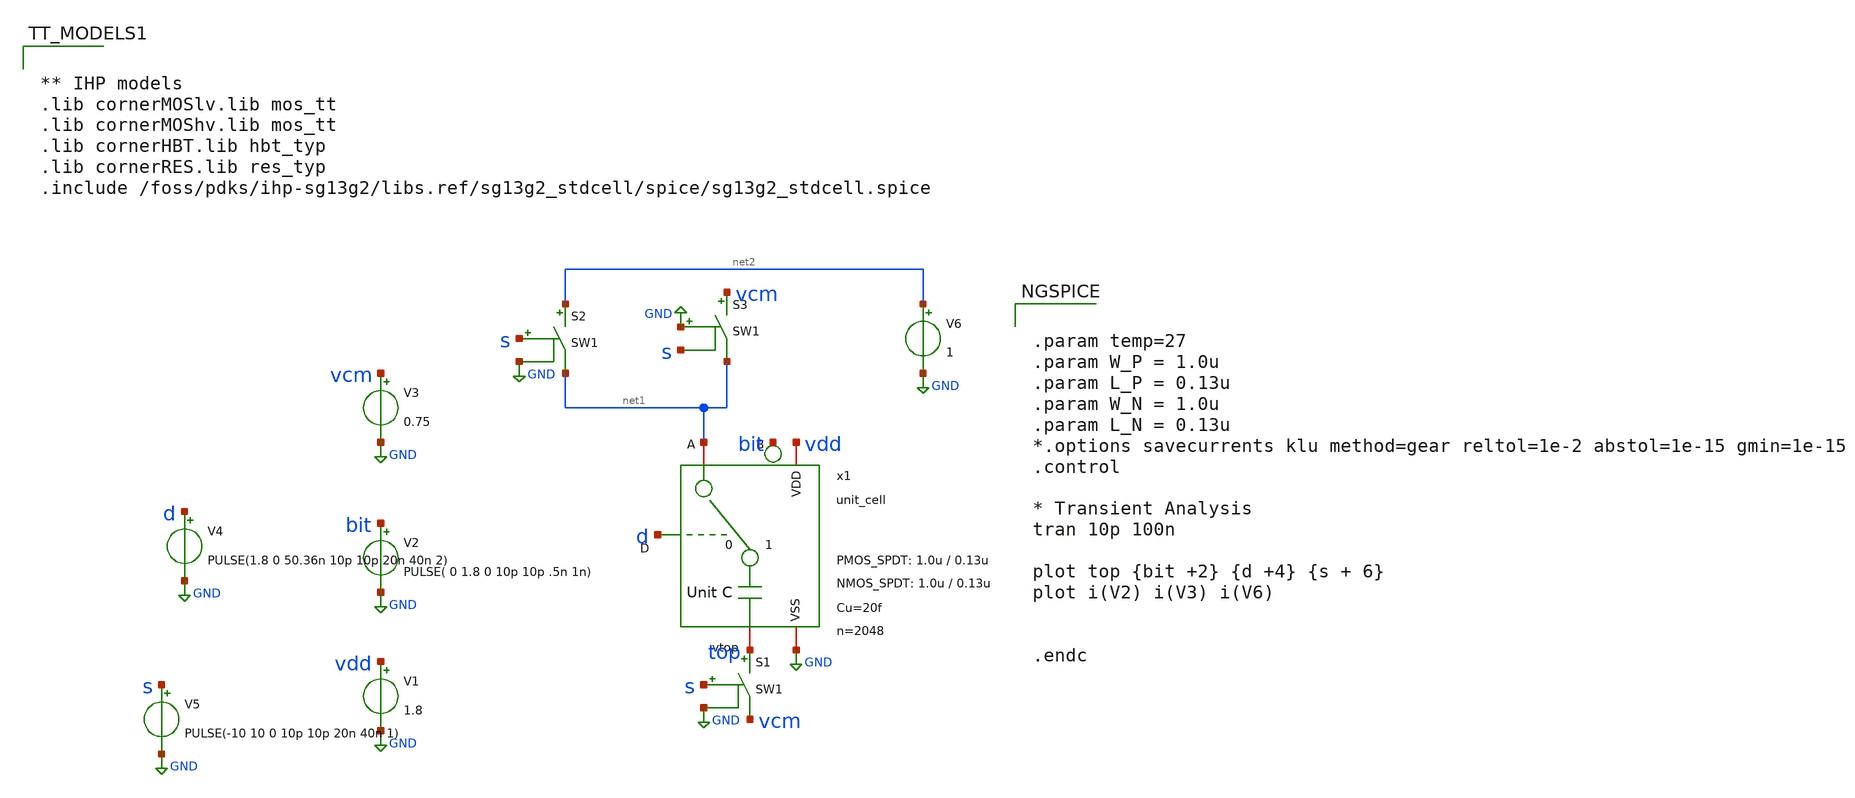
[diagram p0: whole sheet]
** sch_path: xschem/dac_icms_cell/testbenches/tb_unit_cell_tran.sch
* IHP-GmbH/IHP-Open-PDK/ihp-sg13g2/libs.tech/xschem/sg13g2_stdcells/sg13g2_dlygate4sd2_1.sch:
* Copyright 2023 IHP PDK Authors
* Licensed under the Apache License, Version 2.0 (the "License");
**.subckt tb_unit_cell_tran
x1 bit net1 GND d vdd top unit_cell W_P_SPDT=1.0u L_P_SPDT=0.13u W_N_SPDT=1.0u L_N_SPDT=0.13u Cu=20f
+ n=2048
V1 vdd GND 1.8
V2 bit GND PULSE( 0 1.8 0 10p 10p .5n 1n)
V3 vcm GND 0.75
V4 d GND PULSE(1.8 0 50.36n 10p 10p 20n 40n 2)
S1 top vcm s GND SW1
V5 s GND PULSE(-10 10 0 10p 10p 20n 40n 1)
S2 net2 net1 s GND SW1
S3 vcm net1 GND s SW1
V6 net2 GND 1
**** begin user architecture code


.param temp=27
.param W_P = 1.0u
.param L_P = 0.13u
.param W_N = 1.0u
.param L_N = 0.13u
*.options savecurrents klu method=gear reltol=1e-2 abstol=1e-15 gmin=1e-15
.control

* Transient Analysis
tran 10p 100n

plot top {bit +2} {d +4} {s + 6}
plot i(V2) i(V3) i(V6)


.endc




** IHP models
.lib cornerMOSlv.lib mos_tt
.lib cornerMOShv.lib mos_tt
.lib cornerHBT.lib hbt_typ
.lib cornerRES.lib res_typ
.include /foss/pdks/ihp-sg13g2/libs.ref/sg13g2_stdcell/spice/sg13g2_stdcell.spice


**** end user architecture code
**.ends

* expanding   symbol:  dac_icms_cell/unit_cell.sym # of pins=6
** sym_path: xschem/dac_icms_cell/unit_cell.sym
** sch_path: xschem/dac_icms_cell/unit_cell.sch
.subckt unit_cell B A VSS D VDD vtop  W_P_SPDT=1.0u L_P_SPDT=0.13u W_N_SPDT=1.0u L_N_SPDT=0.13u
+ Cu=8f n=1
*.iopin VSS
*.iopin A
*.iopin VDD
*.ipin D
*.iopin B
*.iopin vtop
x1 VDD net3 VSS net1 net2 A dac_switch W_P_TG=3.0u L_P_TG=0.13u W_N_TG=1.0u L_N_TG=0.13u n={1}
C1 net1 vtop Cu m=n
x35 VDD B net2 VSS buffer_lv W_P_INV=10.0u L_P_INV=0.13u W_N_INV=10.0u L_N_INV=0.13u
x2 VDD D net3 VSS buffer_lv W_P_INV=10.0u L_P_INV=0.13u W_N_INV=10.0u L_N_INV=0.13u
.ends


* expanding   symbol:  dac_icms_cell/dac_switch.sym # of pins=6
** sym_path: xschem/dac_icms_cell/dac_switch.sym
** sch_path: xschem/dac_icms_cell/dac_switch.sch
.subckt dac_switch VDD di_spdt_ctrl VSS v_c v_b v_a  W_P_TG=3.0u L_P_TG=0.13u W_N_TG=1.0u
+ L_N_TG=0.13u n=1
*.iopin v_a
*.iopin v_c
*.iopin VDD
*.iopin VSS
*.ipin di_spdt_ctrl
*.iopin v_b
x1 VDD di_spdt_ctrl VSS v_c v_a di_spdt_ctrl_n transmission_gate_lv_w_dummy W_P=W_P_TG L_P=L_P_TG
+ W_N=W_N_TG L_N=L_N_TG W_P_D=1.0u L_P_D=0.13u W_N_D=1.0u L_N_D=0.13u n=n
x8 VDD di_spdt_ctrl di_spdt_ctrl_n VSS inverter_lv W_P=W_P_TG L_P=L_P_TG W_N=W_N_TG L_N=L_N_TG n=1
XM1 net1 v_b VSS VSS sg13_lv_nmos w=0.5u l=0.2u ng=1 m=n mm_ok=1
XM3 net1 v_b VDD VDD sg13_lv_pmos w=1u l=0.2u ng=1 m=n mm_ok=1
x2 VDD net2 VSS net1 v_c net3 transmission_gate_lv_w_dummy W_P=W_P_TG L_P=L_P_TG W_N=W_N_TG
+ L_N=L_N_TG W_P_D=1.0u L_P_D=0.13u W_N_D=1.0u L_N_D=0.13u n=n
x40 net2 di_spdt_ctrl_n VDD VSS sg13g2_dlygate4sd2_1
x4 net3 di_spdt_ctrl VDD VSS sg13g2_dlygate4sd2_1
.ends


* expanding   symbol:  buffer/buffer_lv.sym # of pins=4
** sym_path: buffer/buffer_lv.sym
** sch_path: buffer/buffer_lv.sch
.subckt buffer_lv VDD vin vout VSS  W_P_INV=3.0u L_P_INV=0.13u W_N_INV=1.0u L_N_INV=0.13u
*.ipin vin
*.iopin VDD
*.iopin VSS
*.opin vout
x1 VDD vin net1 VSS inverter_lv W_P=W_P_INV L_P=L_P_INV W_N=W_N_INV L_N=L_N_INV n=1
x2 VDD net1 vout VSS inverter_lv W_P=W_P_INV L_P=L_P_INV W_N=W_N_INV L_N=L_N_INV n=1
.ends


* expanding   symbol:  transmission_gate/transmission_gate_lv_w_dummy.sym # of pins=6
** sym_path: xschem/transmission_gate/transmission_gate_lv_w_dummy.sym
** sch_path: xschem/transmission_gate/transmission_gate_lv_w_dummy.sch
.subckt transmission_gate_lv_w_dummy VDD di_tg_ctrl VSS v_b v_a di_tg_ctrl_n  W_P=2.0u L_P=0.13u
+ W_N=2.0u L_N=0.13u W_P_D=1.0u L_P_D=0.13u W_N_D=1.0u L_N_D=0.13u n=1
*.iopin v_a
*.iopin v_b
*.iopin VDD
*.iopin VSS
*.ipin di_tg_ctrl
*.ipin di_tg_ctrl_n
XM1 v_a di_tg_ctrl v_b VSS sg13_lv_nmos w=W_N l=L_N ng=1 m=n mm_ok=1
XM2 v_a di_tg_ctrl_n v_b VDD sg13_lv_pmos w=W_P l=L_P ng=1 m=n mm_ok=1
XMdummy2 v_b di_tg_ctrl v_b VDD sg13_lv_pmos w=W_P_D l=L_P_D ng=1 m=n mm_ok=1
XMdummy1 v_b di_tg_ctrl_n v_b VSS sg13_lv_nmos w=W_N_D l=L_N_D ng=1 m=n mm_ok=1
.ends


* expanding   symbol:  inverter/inverter_lv.sym # of pins=4
** sym_path: xschem/inverter/inverter_lv.sym
** sch_path: xschem/inverter/inverter_lv.sch
.subckt inverter_lv VDD vin vout VSS  W_P=3.0u L_P=0.13u W_N=1.0u L_N=0.13u n=1
*.ipin vin
*.iopin VDD
*.iopin VSS
*.opin vout
XM1 vout vin VDD VDD sg13_lv_pmos w=W_P l=L_P ng=1 m=n mm_ok=1
XM2 vout vin VSS VSS sg13_lv_nmos w=W_N l=L_N ng=1 m=n mm_ok=1
.ends


* expanding   symbol:  sg13g2_stdcells/sg13g2_dlygate4sd2_1.sym # of pins=2
** sym_path: sg13g2_stdcells/sg13g2_dlygate4sd2_1.sym
** sch_path: sg13g2_stdcells/sg13g2_dlygate4sd2_1.sch
.subckt sg13g2_dlygate4sd2_1 X A VDD VSS
*.ipin A
*.opin X
*.iopin VDD
*.iopin VSS
XM1 net2 A VSS VSS sg13_lv_nmos w=420.00n l=130.00n ng=1 m=1 mm_ok=1
XM2 net1 net2 VSS VSS sg13_lv_nmos w=420.00n l=180.00n ng=1 m=1 mm_ok=1
XM3 net3 net1 VSS VSS sg13_lv_nmos w=420.00n l=180.00n ng=1 m=1 mm_ok=1
XM4 X net3 VSS VSS sg13_lv_nmos w=740.00n l=130.00n ng=1 m=1 mm_ok=1
XM5 net2 A VDD VDD sg13_lv_pmos w=420.00n l=130.00n ng=1 m=1 mm_ok=1
XM6 net1 net2 VDD VDD sg13_lv_pmos w=1.000u l=250.00n ng=1 m=1 mm_ok=1
XM7 net3 net1 VDD VDD sg13_lv_pmos w=1.000u l=250.00n ng=1 m=1 mm_ok=1
XM8 X net3 VDD VDD sg13_lv_pmos w=1.12u l=130.00n ng=1 m=1 mm_ok=1
.ends

.GLOBAL GND
**** begin user architecture code
.MODEL SW1 SW   VT=0.9 VH=0.01  RON=10 ROFF=1G
**** end user architecture code
.end
